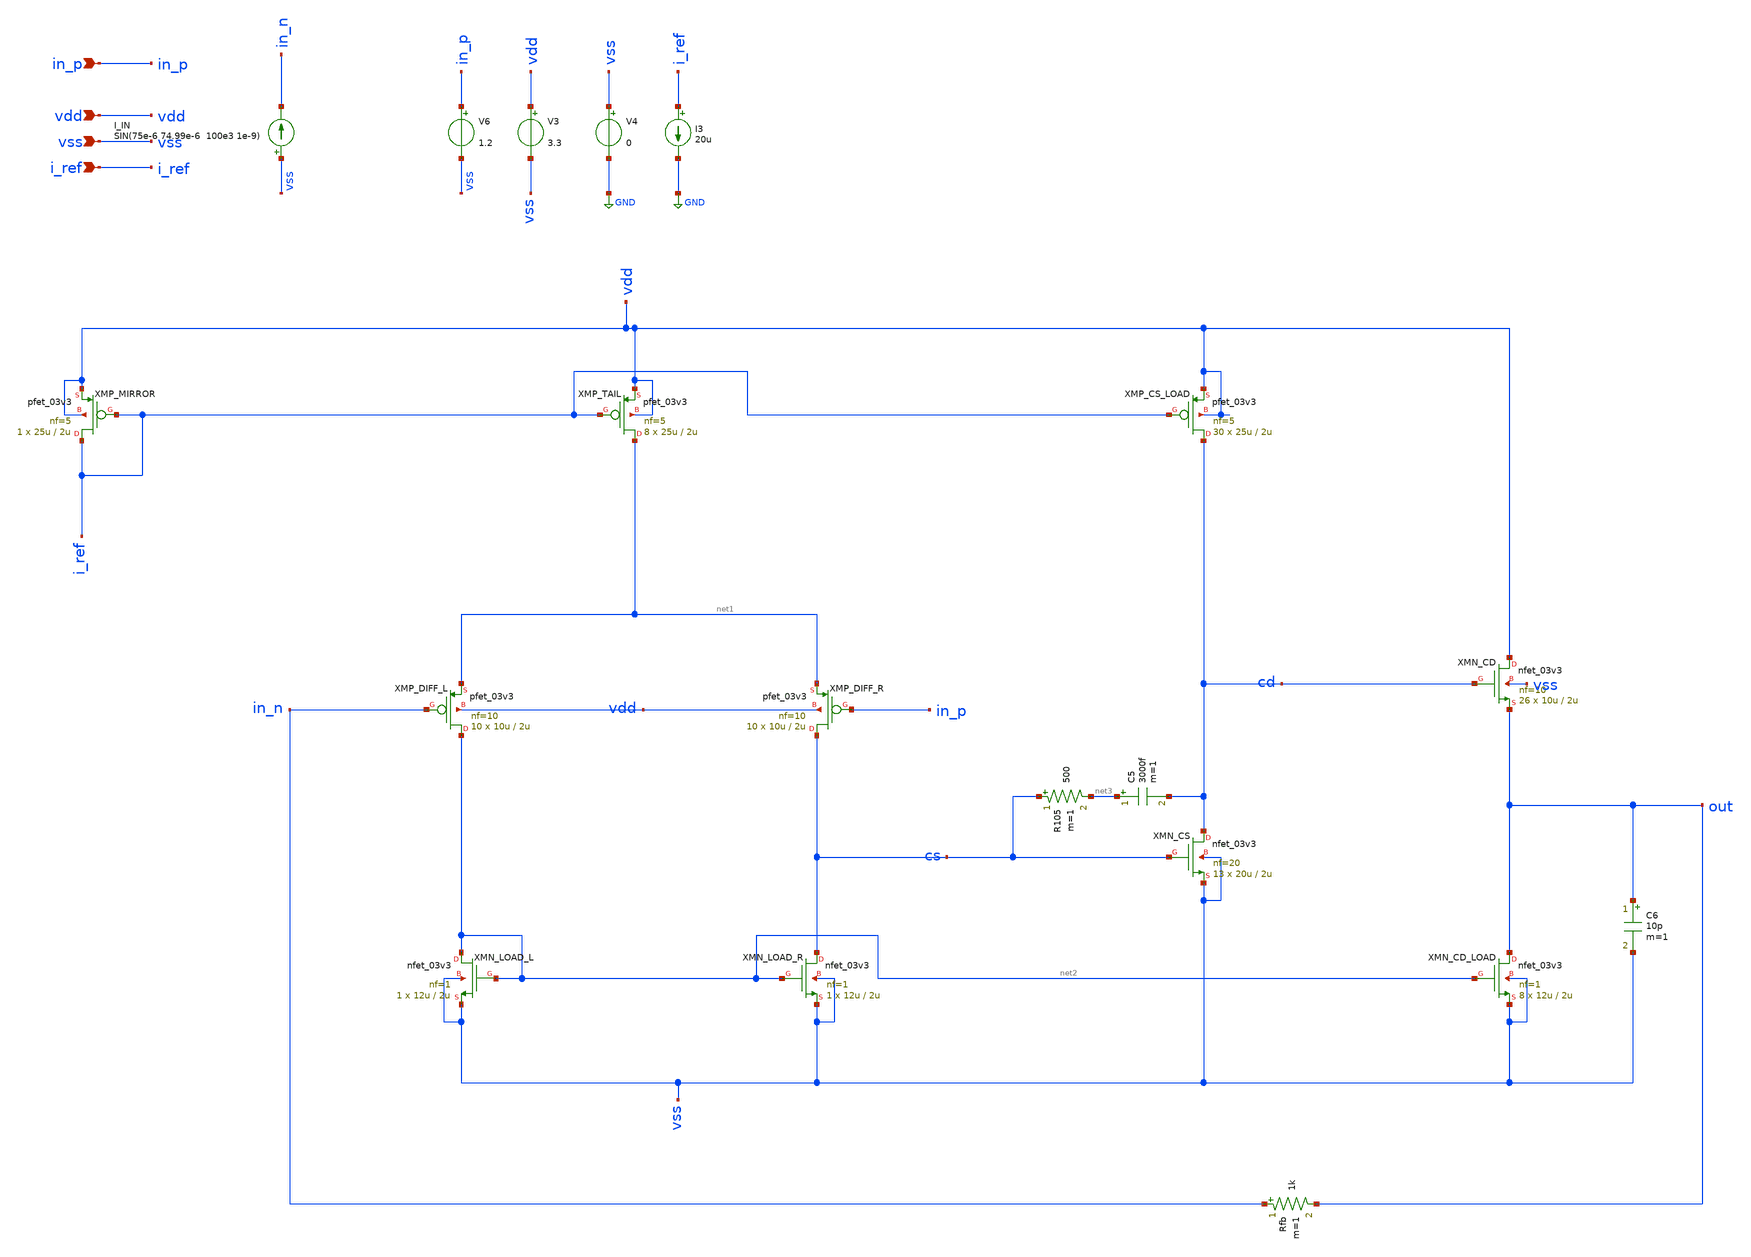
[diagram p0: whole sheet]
** sch_path: designs/libs/TIA/TIA_TB_tran.sch
**.subckt TIA_TB_tran in_p vdd vss i_ref
*.ipin in_p
*.ipin vdd
*.ipin vss
*.ipin i_ref
XMP_TAIL net1 i_ref vdd vdd pfet_03v3 L=2u W=25u nf=5 ad='int((nf+1)/2) * W/nf * 0.18u' as='int((nf+2)/2) * W/nf * 0.18u'
+ pd='2*int((nf+1)/2) * (W/nf + 0.18u)' ps='2*int((nf+2)/2) * (W/nf + 0.18u)' nrd='0.18u / W' nrs='0.18u / W'
+ sa=0 sb=0 sd=0 m=8
XMP_DIFF_L net2 in_n net1 vdd pfet_03v3 L=2u W=10u nf=10 ad='int((nf+1)/2) * W/nf * 0.18u' as='int((nf+2)/2) * W/nf * 0.18u'
+ pd='2*int((nf+1)/2) * (W/nf + 0.18u)' ps='2*int((nf+2)/2) * (W/nf + 0.18u)' nrd='0.18u / W' nrs='0.18u / W'
+ sa=0 sb=0 sd=0 m=10
XMP_DIFF_R cs in_p net1 vdd pfet_03v3 L=2u W=10u nf=10 ad='int((nf+1)/2) * W/nf * 0.18u' as='int((nf+2)/2) * W/nf * 0.18u'
+ pd='2*int((nf+1)/2) * (W/nf + 0.18u)' ps='2*int((nf+2)/2) * (W/nf + 0.18u)' nrd='0.18u / W' nrs='0.18u / W'
+ sa=0 sb=0 sd=0 m=10
XMP_CS_LOAD cd i_ref vdd vdd pfet_03v3 L=2u W=25u nf=5 ad='int((nf+1)/2) * W/nf * 0.18u' as='int((nf+2)/2) * W/nf * 0.18u'
+ pd='2*int((nf+1)/2) * (W/nf + 0.18u)' ps='2*int((nf+2)/2) * (W/nf + 0.18u)' nrd='0.18u / W' nrs='0.18u / W'
+ sa=0 sb=0 sd=0 m=30
XMP_MIRROR i_ref i_ref vdd vdd pfet_03v3 L=2u W=25u nf=5 ad='int((nf+1)/2) * W/nf * 0.18u' as='int((nf+2)/2) * W/nf * 0.18u'
+ pd='2*int((nf+1)/2) * (W/nf + 0.18u)' ps='2*int((nf+2)/2) * (W/nf + 0.18u)' nrd='0.18u / W' nrs='0.18u / W'
+ sa=0 sb=0 sd=0 m=1
XMN_LOAD_R cs net2 vss vss nfet_03v3 L=2u W=12u nf=1 ad='int((nf+1)/2) * W/nf * 0.18u' as='int((nf+2)/2) * W/nf * 0.18u'
+ pd='2*int((nf+1)/2) * (W/nf + 0.18u)' ps='2*int((nf+2)/2) * (W/nf + 0.18u)' nrd='0.18u / W' nrs='0.18u / W'
+ sa=0 sb=0 sd=0 m=1
XMN_LOAD_L net2 net2 vss vss nfet_03v3 L=2u W=12u nf=1 ad='int((nf+1)/2) * W/nf * 0.18u' as='int((nf+2)/2) * W/nf * 0.18u'
+ pd='2*int((nf+1)/2) * (W/nf + 0.18u)' ps='2*int((nf+2)/2) * (W/nf + 0.18u)' nrd='0.18u / W' nrs='0.18u / W'
+ sa=0 sb=0 sd=0 m=1
XMN_CS cd cs vss vss nfet_03v3 L=2u W=20u nf=20 ad='int((nf+1)/2) * W/nf * 0.18u' as='int((nf+2)/2) * W/nf * 0.18u'
+ pd='2*int((nf+1)/2) * (W/nf + 0.18u)' ps='2*int((nf+2)/2) * (W/nf + 0.18u)' nrd='0.18u / W' nrs='0.18u / W'
+ sa=0 sb=0 sd=0 m=13
XMN_CD vdd cd out vss nfet_03v3 L=2u W=10u nf=10 ad='int((nf+1)/2) * W/nf * 0.18u' as='int((nf+2)/2) * W/nf * 0.18u'
+ pd='2*int((nf+1)/2) * (W/nf + 0.18u)' ps='2*int((nf+2)/2) * (W/nf + 0.18u)' nrd='0.18u / W' nrs='0.18u / W'
+ sa=0 sb=0 sd=0 m=26
XMN_CD_LOAD out net2 vss vss nfet_03v3 L=2u W=12u nf=1 ad='int((nf+1)/2) * W/nf * 0.18u' as='int((nf+2)/2) * W/nf * 0.18u'
+ pd='2*int((nf+1)/2) * (W/nf + 0.18u)' ps='2*int((nf+2)/2) * (W/nf + 0.18u)' nrd='0.18u / W' nrs='0.18u / W'
+ sa=0 sb=0 sd=0 m=8
V3 vdd vss 3.3
C5 net3 cd 3000f m=1
R105 cs net3 500 m=1
V4 vss GND 0
V6 in_p vss 1.2
I3 i_ref GND 20u
C6 out vss 10p m=1
Rfb in_n out 1k m=1
I_IN vss in_n SIN(75e-6 74.99e-6 100e3 1e-9)
**** begin user architecture code


.save @m.xmp_mirror.m0[gds]
.save @m.xmp_mirror.m0[gm]
.save @m.xmp_mirror.m0[id]
.save @m.xmp_mirror.m0[vth]
.save @m.xmp_mirror.m0[vdsat]
.save @m.xmp_mirror.m0[vds]


.save @m.xmp_tail.m0[gds]
.save @m.xmp_tail.m0[gm]
.save @m.xmp_tail.m0[id]
.save @m.xmp_tail.m0[vth]
.save @m.xmp_tail.m0[vdsat]
.save @m.xmp_tail.m0[vds]

.save @m.xmp_diff_l.m0[gds]
.save @m.xmp_diff_l.m0[gm]
.save @m.xmp_diff_l.m0[id]
.save @m.xmp_diff_l.m0[vth]
.save @m.xmp_diff_l.m0[vdsat]
.save @m.xmp_diff_l.m0[vds]

.save @m.xmp_diff_r.m0[gds]
.save @m.xmp_diff_r.m0[gm]
.save @m.xmp_diff_r.m0[id]
.save @m.xmp_diff_r.m0[vth]
.save @m.xmp_diff_r.m0[vdsat]
.save @m.xmp_diff_r.m0[vds]

.save @m.xmn_load_l.m0[gds]
.save @m.xmn_load_l.m0[gm]
.save @m.xmn_load_l.m0[id]
.save @m.xmn_load_l.m0[vth]
.save @m.xmn_load_l.m0[vdsat]
.save @m.xmn_load_l.m0[vds]

.save @m.xmn_load_r.m0[gds]
.save @m.xmn_load_r.m0[gm]
.save @m.xmn_load_r.m0[id]
.save @m.xmn_load_r.m0[vth]
.save @m.xmn_load_r.m0[vdsat]
.save @m.xmn_load_r.m0[vds]

.save @m.xmp_cs_load.m0[gds]
.save @m.xmp_cs_load.m0[gm]
.save @m.xmp_cs_load.m0[id]
.save @m.xmp_cs_load.m0[vth]
.save @m.xmp_cs_load.m0[vdsat]
.save @m.xmp_cs_load.m0[vds]

.save @m.xmn_cs.m0[gds]
.save @m.xmn_cs.m0[gm]
.save @m.xmn_cs.m0[id]
.save @m.xmn_cs.m0[vth]
.save @m.xmn_cs.m0[vdsat]
.save @m.xmn_cs.m0[vds]

.save @m.xmn_cd_load.m0[gds]
.save @m.xmn_cd_load.m0[gm]
.save @m.xmn_cd_load.m0[id]
.save @m.xmn_cd_load.m0[vth]
.save @m.xmn_cd_load.m0[vdsat]
.save @m.xmn_cd_load.m0[vds]

.save @m.xmn_cd.m0[gds]
.save @m.xmn_cd.m0[gm]
.save @m.xmn_cd.m0[id]
.save @m.xmn_cd.m0[vth]
.save @m.xmn_cd.m0[vdsat]
.save @m.xmn_cd.m0[vds]







.control
save all


** Simulation

let tstop = 60e-6
let tstep = 1e-9

op

tran $&tstep $&tstop

write TIA_TB_tran.raw

** Plots

setplot tran1
let v_out = v(out)

let i_in = -(v(out)-v(in_n))/1e3

plot v_out

plot i_in



setplot op1
print @m.xmp_mirror.m0[id]
print cs
print cd
print out

print @m.xmn_cs.m0[vdsat]
print @m.xmn_cs.m0[vds]

print @m.xmp_cs_load.m0[vdsat]
print @m.xmp_cs_load.m0[vds]

print @m.xmn_cd.m0[vdsat]
print @m.xmn_cd.m0[vds]

print @m.xmn_cd_load.m0[vdsat]
print @m.xmn_cd_load.m0[vds]






.endc



.include $::180MCU_MODELS/design.ngspice
.lib $::180MCU_MODELS/sm141064.ngspice typical

**** end user architecture code
**.ends
.GLOBAL GND
.end
